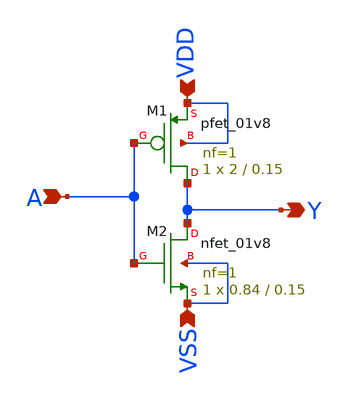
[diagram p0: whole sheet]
** sch_path: buffer/design_circuit/invx2.sch
**.subckt invx2 A Y VDD VSS
*.ipin A
*.opin Y
*.ipin VDD
*.ipin VSS
XM1 Y A VDD VDD sky130_fd_pr__pfet_01v8 L=0.15 W=2 nf=1 ad='int((nf+1)/2) * W/nf * 0.29' as='int((nf+2)/2) * W/nf * 0.29'
+ pd='2*int((nf+1)/2) * (W/nf + 0.29)' ps='2*int((nf+2)/2) * (W/nf + 0.29)' nrd='0.29 / W' nrs='0.29 / W'
+ sa=0 sb=0 sd=0 mult=1 m=1
XM2 Y A VSS VSS sky130_fd_pr__nfet_01v8 L=0.15 W=0.84 nf=1 ad='int((nf+1)/2) * W/nf * 0.29' as='int((nf+2)/2) * W/nf * 0.29'
+ pd='2*int((nf+1)/2) * (W/nf + 0.29)' ps='2*int((nf+2)/2) * (W/nf + 0.29)' nrd='0.29 / W' nrs='0.29 / W'
+ sa=0 sb=0 sd=0 mult=1 m=1
**.ends
.end
